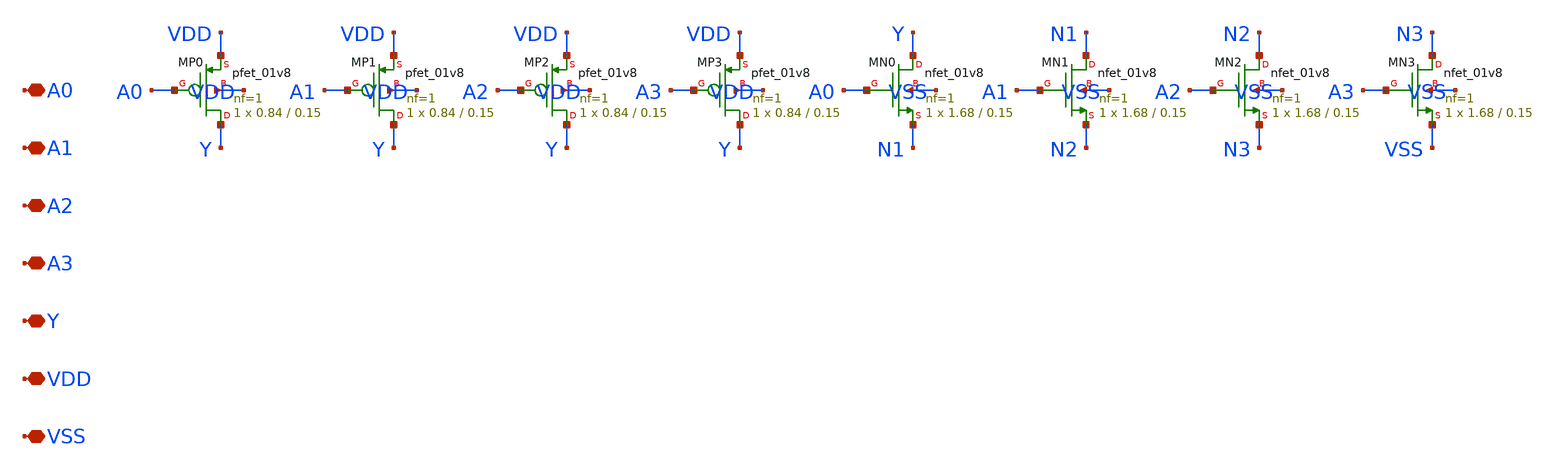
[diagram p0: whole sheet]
** sch_path: design/compiler/cells/sram_nand4.sch
**.subckt sram_nand4 A0 A1 A2 A3 Y VDD VSS
*.iopin A0
*.iopin A1
*.iopin A2
*.iopin A3
*.iopin Y
*.iopin VDD
*.iopin VSS
XMP0 Y A0 VDD VDD sky130_fd_pr__pfet_01v8 L=0.15 W=0.84 nf=1 ad=0.2436 as=0.2436 pd=2.26 ps=2.26
+ nrd=0.3452 nrs=0.3452 sa=0 sb=0 sd=0 mult=1 m=1
XMP1 Y A1 VDD VDD sky130_fd_pr__pfet_01v8 L=0.15 W=0.84 nf=1 ad=0.2436 as=0.2436 pd=2.26 ps=2.26
+ nrd=0.3452 nrs=0.3452 sa=0 sb=0 sd=0 mult=1 m=1
XMP2 Y A2 VDD VDD sky130_fd_pr__pfet_01v8 L=0.15 W=0.84 nf=1 ad=0.2436 as=0.2436 pd=2.26 ps=2.26
+ nrd=0.3452 nrs=0.3452 sa=0 sb=0 sd=0 mult=1 m=1
XMP3 Y A3 VDD VDD sky130_fd_pr__pfet_01v8 L=0.15 W=0.84 nf=1 ad=0.2436 as=0.2436 pd=2.26 ps=2.26
+ nrd=0.3452 nrs=0.3452 sa=0 sb=0 sd=0 mult=1 m=1
XMN0 Y A0 N1 VSS sky130_fd_pr__nfet_01v8 L=0.15 W=1.68 nf=1 ad=0.4872 as=0.4872 pd=3.94 ps=3.94
+ nrd=0.1726 nrs=0.1726 sa=0 sb=0 sd=0 mult=1 m=1
XMN1 N1 A1 N2 VSS sky130_fd_pr__nfet_01v8 L=0.15 W=1.68 nf=1 ad=0.4872 as=0.4872 pd=3.94 ps=3.94
+ nrd=0.1726 nrs=0.1726 sa=0 sb=0 sd=0 mult=1 m=1
XMN2 N2 A2 N3 VSS sky130_fd_pr__nfet_01v8 L=0.15 W=1.68 nf=1 ad=0.4872 as=0.4872 pd=3.94 ps=3.94
+ nrd=0.1726 nrs=0.1726 sa=0 sb=0 sd=0 mult=1 m=1
XMN3 N3 A3 VSS VSS sky130_fd_pr__nfet_01v8 L=0.15 W=1.68 nf=1 ad=0.4872 as=0.4872 pd=3.94 ps=3.94
+ nrd=0.1726 nrs=0.1726 sa=0 sb=0 sd=0 mult=1 m=1
**.ends
.end
